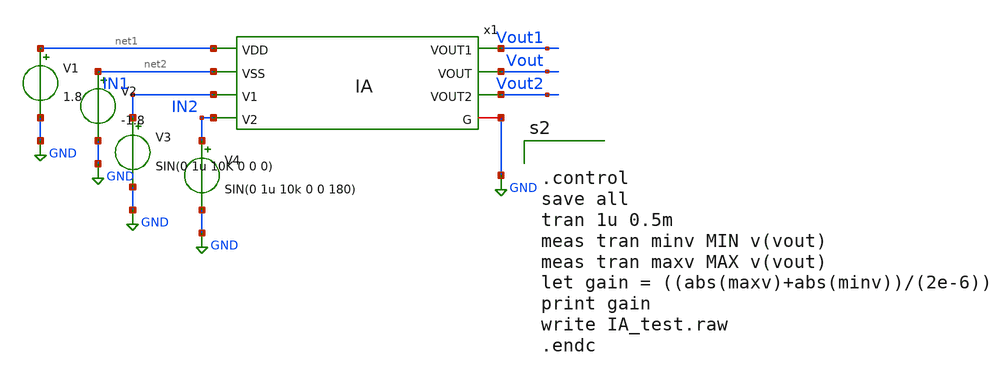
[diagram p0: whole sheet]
** sch_path: xschem/IA_test.sch
**.subckt IA_test
V1 net1 GND 1.8
V2 net2 GND -1.8
V3 IN1 GND SIN(0 1u 10K 0 0 0)
V4 IN2 GND SIN(0 1u 10k 0 0 180)
x1 Vout1 net1 net2 Vout IN1 IN2 Vout2 GND IA
**** begin user architecture code

** opencircuitdesign pdks install
.lib $::SKYWATER_MODELS/sky130.lib.spice tt




.control
save all
tran 1u 0.5m
meas tran minv MIN v(vout)
meas tran maxv MAX v(vout)
let gain = ((abs(maxv)+abs(minv))/(2e-6))
print gain
write IA_test.raw
.endc

**** end user architecture code
**.ends

* expanding   symbol:  /home/caonam/OpenLane/FINALPROJECT/sky130_hcmus_ip__instramp/xschem/IA.sym #
*+ of pins=8
** sym_path: xschem/IA.sym
** sch_path: xschem/IA.sch
.subckt IA VOUT1 VDD VSS VOUT V1 V2 VOUT2 G
*.opin VOUT
*.iopin G
*.ipin VDD
*.ipin VSS
*.ipin V1
*.ipin V2
*.opin VOUT1
*.opin VOUT2
XR3 net5 net6 G sky130_fd_pr__res_high_po W=1 L=61.9 mult=20 m=20
XR1 net7 net8 G sky130_fd_pr__res_high_po W=1 L=61.9 mult=20 m=20
XR4 net9 net10 G sky130_fd_pr__res_high_po W=1 L=61.9 mult=20 m=20
XR5 net11 net12 G sky130_fd_pr__res_high_po W=1 L=61.9 mult=20 m=20
XR6 net13 net14 G sky130_fd_pr__res_high_po W=1 L=61.9 mult=20 m=20
XR8 net15 net16 G sky130_fd_pr__res_high_po W=1 L=61.9 mult=20 m=20
XR9 net17 net18 G sky130_fd_pr__res_high_po W=1 L=200.7 mult=4 m=4
XR10 net19 net20 G sky130_fd_pr__res_high_po W=1 L=200.7 mult=4 m=4
XR11 net21 net22 G sky130_fd_pr__res_high_po W=1 L=200.7 mult=4 m=4
XR12 net23 net24 G sky130_fd_pr__res_high_po W=1 L=200.7 mult=4 m=4
XR13 net25 net26 G sky130_fd_pr__res_high_po W=1 L=61.9 mult=20 m=20
x1 VDD VSS V2 net3 VOUT1 opamp
x2 VDD VSS V1 net4 VOUT2 opamp
x3 VDD VSS net2 net1 VOUT opamp
R2 VOUT1 net3 2k m=1
R7 net3 net4 1k m=1
R14 VOUT2 net2 1k m=1
R15 VOUT1 net1 1k m=1
R16 net4 VOUT2 2k m=1
R17 net1 VOUT 64k m=1
R18 net2 G 64k m=1
.ends


* expanding   symbol:  ../xschem/opamp.sym # of pins=5
** sym_path: xschem/opamp.sym
** sch_path: xschem/opamp.sch
.subckt opamp VDD VSS V1 V2 VOUT
*.ipin VSS
*.ipin VDD
*.ipin V2
*.ipin V1
*.opin VOUT
XM2 net5 V2 net1 VSS sky130_fd_pr__nfet_01v8 L=1 W=8.5 nf=1 ad='int((nf+1)/2) * W/nf * 0.29' as='int((nf+2)/2) * W/nf * 0.29'
+ pd='2*int((nf+1)/2) * (W/nf + 0.29)' ps='2*int((nf+2)/2) * (W/nf + 0.29)' nrd='0.29 / W' nrs='0.29 / W'
+ sa=0 sb=0 sd=0 mult=1 m=1
XM1 net6 net5 VDD VDD sky130_fd_pr__pfet_01v8 L=1 W=41 nf=1 ad='int((nf+1)/2) * W/nf * 0.29' as='int((nf+2)/2) * W/nf * 0.29'
+ pd='2*int((nf+1)/2) * (W/nf + 0.29)' ps='2*int((nf+2)/2) * (W/nf + 0.29)' nrd='0.29 / W' nrs='0.29 / W'
+ sa=0 sb=0 sd=0 mult=1 m=1
XM4 net6 V1 net1 VSS sky130_fd_pr__nfet_01v8 L=1 W=8.5 nf=1 ad='int((nf+1)/2) * W/nf * 0.29' as='int((nf+2)/2) * W/nf * 0.29'
+ pd='2*int((nf+1)/2) * (W/nf + 0.29)' ps='2*int((nf+2)/2) * (W/nf + 0.29)' nrd='0.29 / W' nrs='0.29 / W'
+ sa=0 sb=0 sd=0 mult=1 m=1
XM5 net1 net4 VSS VSS sky130_fd_pr__nfet_01v8 L=1 W=20 nf=1 ad='int((nf+1)/2) * W/nf * 0.29' as='int((nf+2)/2) * W/nf * 0.29'
+ pd='2*int((nf+1)/2) * (W/nf + 0.29)' ps='2*int((nf+2)/2) * (W/nf + 0.29)' nrd='0.29 / W' nrs='0.29 / W'
+ sa=0 sb=0 sd=0 mult=1 m=1
XM6 VOUT net4 VSS VSS sky130_fd_pr__nfet_01v8 L=1 W=19 nf=1 ad='int((nf+1)/2) * W/nf * 0.29' as='int((nf+2)/2) * W/nf * 0.29'
+ pd='2*int((nf+1)/2) * (W/nf + 0.29)' ps='2*int((nf+2)/2) * (W/nf + 0.29)' nrd='0.29 / W' nrs='0.29 / W'
+ sa=0 sb=0 sd=0 mult=1 m=1
XM7 net4 net4 VSS VSS sky130_fd_pr__nfet_01v8 L=1 W=20 nf=1 ad='int((nf+1)/2) * W/nf * 0.29' as='int((nf+2)/2) * W/nf * 0.29'
+ pd='2*int((nf+1)/2) * (W/nf + 0.29)' ps='2*int((nf+2)/2) * (W/nf + 0.29)' nrd='0.29 / W' nrs='0.29 / W'
+ sa=0 sb=0 sd=0 mult=1 m=1
XM3 net5 net5 VDD VDD sky130_fd_pr__pfet_01v8 L=1 W=41 nf=1 ad='int((nf+1)/2) * W/nf * 0.29' as='int((nf+2)/2) * W/nf * 0.29'
+ pd='2*int((nf+1)/2) * (W/nf + 0.29)' ps='2*int((nf+2)/2) * (W/nf + 0.29)' nrd='0.29 / W' nrs='0.29 / W'
+ sa=0 sb=0 sd=0 mult=1 m=1
XM8 VOUT net6 VDD VDD sky130_fd_pr__pfet_01v8 L=1 W=40 nf=1 ad='int((nf+1)/2) * W/nf * 0.29' as='int((nf+2)/2) * W/nf * 0.29'
+ pd='2*int((nf+1)/2) * (W/nf + 0.29)' ps='2*int((nf+2)/2) * (W/nf + 0.29)' nrd='0.29 / W' nrs='0.29 / W'
+ sa=0 sb=0 sd=0 mult=2 m=2
XR3 net2 VDD VSS sky130_fd_pr__res_high_po W=1 L=50 mult=1 m=1
XR1 net3 net2 VSS sky130_fd_pr__res_high_po W=1 L=50 mult=1 m=1
XR2 net4 net3 VSS sky130_fd_pr__res_high_po W=1 L=50 mult=1 m=1
XR4 net7 VOUT VSS sky130_fd_pr__res_high_po W=1 L=7 mult=1 m=1
XC1 net7 net6 sky130_fd_pr__cap_mim_m3_1 W=5.55 L=10 MF=20 m=20
.ends

.GLOBAL GND
.end
